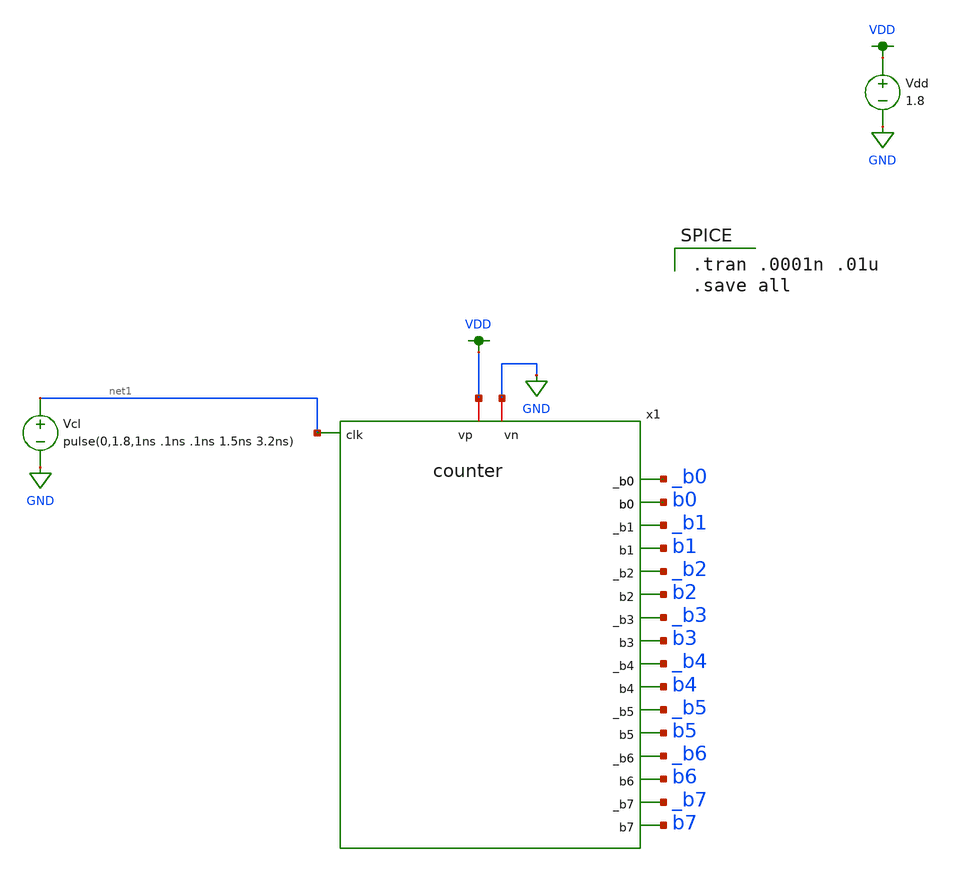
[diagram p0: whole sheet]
** sch_path: xschem/counter_testbench.sch
**.subckt counter_testbench
Vdd VDD GND 1.8
Vcl net1 GND pulse(0,1.8,1ns .1ns .1ns 1.5ns 3.2ns)
x1 VDD GND net1 _b1 b1 _b2 b2 _b3 b3 _b0 b0 _b5 b5 _b6 b6 _b7 b7 _b4 b4 counter
**** begin user architecture code

.option wnflag=1
.param MC_SWITCH=1.0
.lib ~/skywater/skywater-pdk/libraries/sky130_fd_pr_ngspice/latest/models/sky130.lib.spice tt


.tran .0001n .01u
.save all

**** end user architecture code
**.ends

* expanding   symbol:  /home/madvlsi/dev/git/magic-dds/xschem/logic_gates/counter.sym # of pins=19
** sym_path: xschem/logic_gates/counter.sym
** sch_path: xschem/logic_gates/counter.sch
.subckt counter vp vn clk _b1 b1 _b2 b2 _b3 b3 _b0 b0 _b5 b5 _b6 b6 _b7 b7 _b4 b4
*.iopin vp
*.iopin vn
*.ipin clk
*.opin b0
*.opin _b0
*.opin b1
*.opin _b1
*.opin b2
*.opin _b2
*.opin b3
*.opin _b3
*.opin b4
*.opin _b4
*.opin b5
*.opin _b5
*.opin b6
*.opin _b6
*.opin b7
*.opin _b7
X2 _b1 b1 _b1 b1 _b0 vp vn dflipflop
X3 _b2 b2 _b2 b2 _b1 vp vn dflipflop
X4 _b3 b3 _b3 b3 _b2 vp vn dflipflop
X5 _b4 b4 _b4 b4 _b3 vp vn dflipflop
X6 _b5 b5 _b5 b5 _b4 vp vn dflipflop
X7 _b6 b6 _b6 b6 _b5 vp vn dflipflop
X8 _b7 b7 _b7 b7 _b6 vp vn dflipflop
X1 _b0 b0 _b0 b0 clk vp vn dflipflop
.ends


* expanding   symbol:  /home/madvlsi/dev/git/magic-dds/xschem/logic_gates/dflipflop.sym # of pins=7
** sym_path: xschem/logic_gates/dflipflop.sym
** sch_path: xschem/logic_gates/dflipflop.sch
.subckt dflipflop q_bar q d d_bar clk vp vn
*.opin q
*.opin q_bar
*.iopin vp
*.iopin vn
*.ipin d_bar
*.ipin d
*.ipin clk
XM8 vp net2 net3 vp sky130_fd_pr__pfet_01v8 L=0.15 W=1 nf=1 ad='int((nf+1)/2) * W/nf * 0.29' as='int((nf+2)/2) * W/nf * 0.29'
+ pd='2*int((nf+1)/2) * (W/nf + 0.29)' ps='2*int((nf+2)/2) * (W/nf + 0.29)' nrd='0.29 / W' nrs='0.29 / W'
+ sa=0 sb=0 sd=0 mult=1 m=1
XM9 vp net3 net2 vp sky130_fd_pr__pfet_01v8 L=0.15 W=1 nf=1 ad='int((nf+1)/2) * W/nf * 0.29' as='int((nf+2)/2) * W/nf * 0.29'
+ pd='2*int((nf+1)/2) * (W/nf + 0.29)' ps='2*int((nf+2)/2) * (W/nf + 0.29)' nrd='0.29 / W' nrs='0.29 / W'
+ sa=0 sb=0 sd=0 mult=1 m=1
XM5 net1 clk vn vn sky130_fd_pr__nfet_01v8 L=0.15 W=1 nf=1 ad='int((nf+1)/2) * W/nf * 0.29' as='int((nf+2)/2) * W/nf * 0.29'
+ pd='2*int((nf+1)/2) * (W/nf + 0.29)' ps='2*int((nf+2)/2) * (W/nf + 0.29)' nrd='0.29 / W' nrs='0.29 / W'
+ sa=0 sb=0 sd=0 mult=1 m=1
XM6 net3 net2 net1 vn sky130_fd_pr__nfet_01v8 L=0.15 W=1 nf=1 ad='int((nf+1)/2) * W/nf * 0.29' as='int((nf+2)/2) * W/nf * 0.29'
+ pd='2*int((nf+1)/2) * (W/nf + 0.29)' ps='2*int((nf+2)/2) * (W/nf + 0.29)' nrd='0.29 / W' nrs='0.29 / W'
+ sa=0 sb=0 sd=0 mult=1 m=1
XM7 net2 net3 net1 vn sky130_fd_pr__nfet_01v8 L=0.15 W=1 nf=1 ad='int((nf+1)/2) * W/nf * 0.29' as='int((nf+2)/2) * W/nf * 0.29'
+ pd='2*int((nf+1)/2) * (W/nf + 0.29)' ps='2*int((nf+2)/2) * (W/nf + 0.29)' nrd='0.29 / W' nrs='0.29 / W'
+ sa=0 sb=0 sd=0 mult=1 m=1
XM13 vn q q_bar vn sky130_fd_pr__nfet_01v8 L=0.15 W=1 nf=1 ad='int((nf+1)/2) * W/nf * 0.29' as='int((nf+2)/2) * W/nf * 0.29'
+ pd='2*int((nf+1)/2) * (W/nf + 0.29)' ps='2*int((nf+2)/2) * (W/nf + 0.29)' nrd='0.29 / W' nrs='0.29 / W'
+ sa=0 sb=0 sd=0 mult=1 m=1
XM3 q clk net2 vn sky130_fd_pr__nfet_01v8 L=0.30 W=1 nf=1 ad='int((nf+1)/2) * W/nf * 0.29' as='int((nf+2)/2) * W/nf * 0.29'
+ pd='2*int((nf+1)/2) * (W/nf + 0.29)' ps='2*int((nf+2)/2) * (W/nf + 0.29)' nrd='0.29 / W' nrs='0.29 / W'
+ sa=0 sb=0 sd=0 mult=1 m=1
XM4 q_bar clk net3 vn sky130_fd_pr__nfet_01v8 L=0.30 W=1 nf=1 ad='int((nf+1)/2) * W/nf * 0.29' as='int((nf+2)/2) * W/nf * 0.29'
+ pd='2*int((nf+1)/2) * (W/nf + 0.29)' ps='2*int((nf+2)/2) * (W/nf + 0.29)' nrd='0.29 / W' nrs='0.29 / W'
+ sa=0 sb=0 sd=0 mult=1 m=1
XM14 vn q_bar q vn sky130_fd_pr__nfet_01v8 L=0.15 W=1 nf=1 ad='int((nf+1)/2) * W/nf * 0.29' as='int((nf+2)/2) * W/nf * 0.29'
+ pd='2*int((nf+1)/2) * (W/nf + 0.29)' ps='2*int((nf+2)/2) * (W/nf + 0.29)' nrd='0.29 / W' nrs='0.29 / W'
+ sa=0 sb=0 sd=0 mult=1 m=1
XM10 net4 clk vp vp sky130_fd_pr__pfet_01v8 L=0.15 W=1 nf=1 ad='int((nf+1)/2) * W/nf * 0.29' as='int((nf+2)/2) * W/nf * 0.29'
+ pd='2*int((nf+1)/2) * (W/nf + 0.29)' ps='2*int((nf+2)/2) * (W/nf + 0.29)' nrd='0.29 / W' nrs='0.29 / W'
+ sa=0 sb=0 sd=0 mult=1 m=1
XM11 q_bar q net4 vp sky130_fd_pr__pfet_01v8 L=0.15 W=1 nf=1 ad='int((nf+1)/2) * W/nf * 0.29' as='int((nf+2)/2) * W/nf * 0.29'
+ pd='2*int((nf+1)/2) * (W/nf + 0.29)' ps='2*int((nf+2)/2) * (W/nf + 0.29)' nrd='0.29 / W' nrs='0.29 / W'
+ sa=0 sb=0 sd=0 mult=1 m=1
XM12 q q_bar net4 vp sky130_fd_pr__pfet_01v8 L=0.15 W=1 nf=1 ad='int((nf+1)/2) * W/nf * 0.29' as='int((nf+2)/2) * W/nf * 0.29'
+ pd='2*int((nf+1)/2) * (W/nf + 0.29)' ps='2*int((nf+2)/2) * (W/nf + 0.29)' nrd='0.29 / W' nrs='0.29 / W'
+ sa=0 sb=0 sd=0 mult=1 m=1
XM15 net1 clk vn vn sky130_fd_pr__nfet_01v8 L=0.15 W=1 nf=1 ad='int((nf+1)/2) * W/nf * 0.29' as='int((nf+2)/2) * W/nf * 0.29'
+ pd='2*int((nf+1)/2) * (W/nf + 0.29)' ps='2*int((nf+2)/2) * (W/nf + 0.29)' nrd='0.29 / W' nrs='0.29 / W'
+ sa=0 sb=0 sd=0 mult=1 m=1
XM16 net4 clk vp vp sky130_fd_pr__pfet_01v8 L=0.15 W=1 nf=1 ad='int((nf+1)/2) * W/nf * 0.29' as='int((nf+2)/2) * W/nf * 0.29'
+ pd='2*int((nf+1)/2) * (W/nf + 0.29)' ps='2*int((nf+2)/2) * (W/nf + 0.29)' nrd='0.29 / W' nrs='0.29 / W'
+ sa=0 sb=0 sd=0 mult=1 m=1
XM1 net2 clk d vp sky130_fd_pr__pfet_01v8 L=0.30 W=1 nf=1 ad='int((nf+1)/2) * W/nf * 0.29' as='int((nf+2)/2) * W/nf * 0.29'
+ pd='2*int((nf+1)/2) * (W/nf + 0.29)' ps='2*int((nf+2)/2) * (W/nf + 0.29)' nrd='0.29 / W' nrs='0.29 / W'
+ sa=0 sb=0 sd=0 mult=1 m=1
XM2 net3 clk d_bar vp sky130_fd_pr__pfet_01v8 L=0.30 W=1 nf=1 ad='int((nf+1)/2) * W/nf * 0.29' as='int((nf+2)/2) * W/nf * 0.29'
+ pd='2*int((nf+1)/2) * (W/nf + 0.29)' ps='2*int((nf+2)/2) * (W/nf + 0.29)' nrd='0.29 / W' nrs='0.29 / W'
+ sa=0 sb=0 sd=0 mult=1 m=1
.ends

.GLOBAL VDD
.GLOBAL GND
.end
